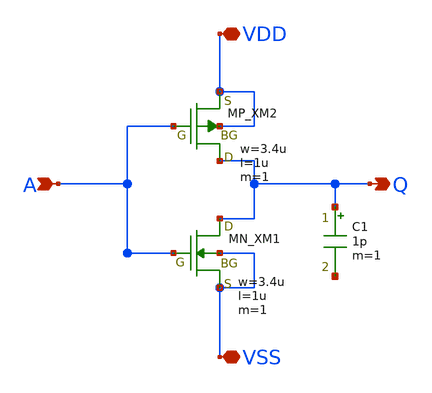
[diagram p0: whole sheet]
** sch_path: member_project/inverter/RISE-A/jijinbei/inverter_tb.sch
**.subckt inverter_tb A Q VSS VDD
*.ipin A
*.opin Q
*.iopin VSS
*.iopin VDD
XXM1 Q A VSS VSS NMOS w=3.4u l=1u nrd=0 nrs=0 m=1
XXM2 Q A VDD VDD PMOS w=3.4u l=1u nrd=0 nrs=0 m=1
C1 Q net1 1p m=1
**.ends
.end
